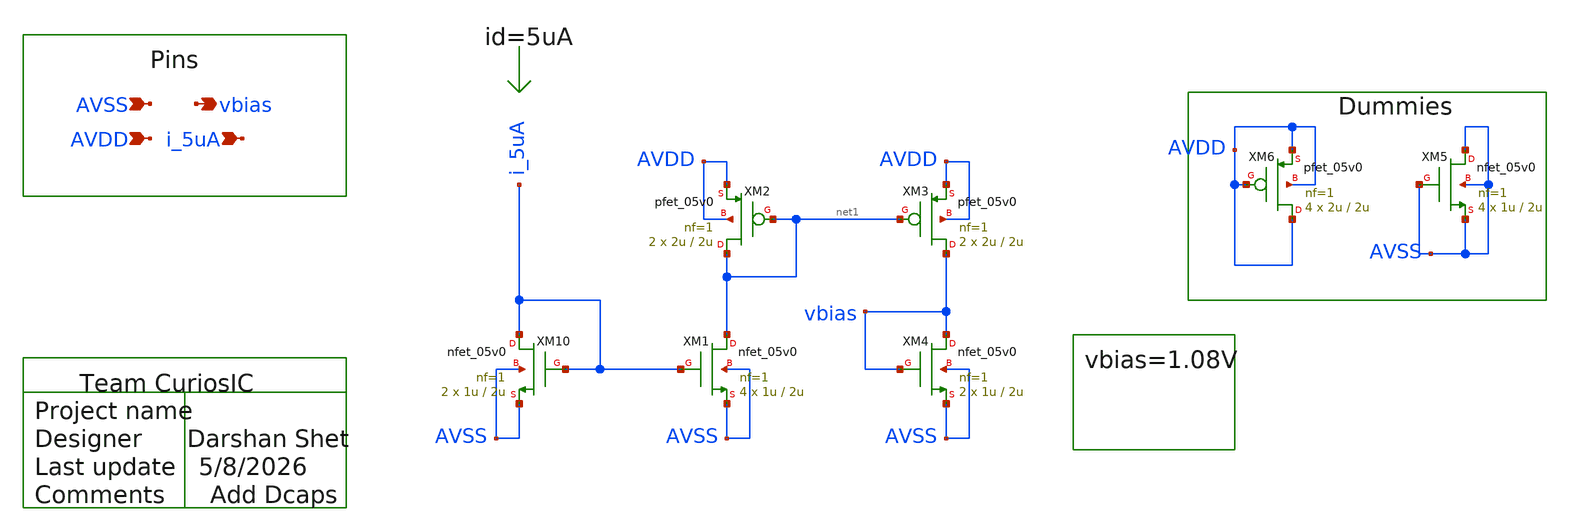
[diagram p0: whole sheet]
** sch_path: design/schematics/ADC/DSM_Loop_filter/First_int/OTA_Files/DS_cic_bms_afe_iadc_first_int_OTA_bias_ckt.sch
**.subckt DS_cic_bms_afe_iadc_first_int_OTA_bias_ckt vbias AVSS AVDD i_5uA
*.opin vbias
*.ipin AVSS
*.ipin AVDD
*.ipin i_5uA
XM10 i_5uA i_5uA AVSS AVSS nfet_05v0 L=2u W=1u nf=1 ad='int((nf+1)/2) * W/nf * 0.18u' as='int((nf+2)/2) * W/nf * 0.18u'
+ pd='2*int((nf+1)/2) * (W/nf + 0.18u)' ps='2*int((nf+2)/2) * (W/nf + 0.18u)' nrd='0.18u / W' nrs='0.18u / W'
+ sa=0 sb=0 sd=0 m=2
XM1 net1 i_5uA AVSS AVSS nfet_05v0 L=2u W=1u nf=1 ad='int((nf+1)/2) * W/nf * 0.18u' as='int((nf+2)/2) * W/nf * 0.18u'
+ pd='2*int((nf+1)/2) * (W/nf + 0.18u)' ps='2*int((nf+2)/2) * (W/nf + 0.18u)' nrd='0.18u / W' nrs='0.18u / W'
+ sa=0 sb=0 sd=0 m=4
XM2 net1 net1 AVDD AVDD pfet_05v0 L=2u W=2u nf=1 ad='int((nf+1)/2) * W/nf * 0.18u' as='int((nf+2)/2) * W/nf * 0.18u'
+ pd='2*int((nf+1)/2) * (W/nf + 0.18u)' ps='2*int((nf+2)/2) * (W/nf + 0.18u)' nrd='0.18u / W' nrs='0.18u / W'
+ sa=0 sb=0 sd=0 m=2
XM3 vbias net1 AVDD AVDD pfet_05v0 L=2u W=2u nf=1 ad='int((nf+1)/2) * W/nf * 0.18u' as='int((nf+2)/2) * W/nf * 0.18u'
+ pd='2*int((nf+1)/2) * (W/nf + 0.18u)' ps='2*int((nf+2)/2) * (W/nf + 0.18u)' nrd='0.18u / W' nrs='0.18u / W'
+ sa=0 sb=0 sd=0 m=2
XM4 vbias vbias AVSS AVSS nfet_05v0 L=2u W=1u nf=1 ad='int((nf+1)/2) * W/nf * 0.18u' as='int((nf+2)/2) * W/nf * 0.18u'
+ pd='2*int((nf+1)/2) * (W/nf + 0.18u)' ps='2*int((nf+2)/2) * (W/nf + 0.18u)' nrd='0.18u / W' nrs='0.18u / W'
+ sa=0 sb=0 sd=0 m=2
XM5 AVSS AVSS AVSS AVSS nfet_05v0 L=2u W=1u nf=1 ad='int((nf+1)/2) * W/nf * 0.18u' as='int((nf+2)/2) * W/nf * 0.18u'
+ pd='2*int((nf+1)/2) * (W/nf + 0.18u)' ps='2*int((nf+2)/2) * (W/nf + 0.18u)' nrd='0.18u / W' nrs='0.18u / W'
+ sa=0 sb=0 sd=0 m=4
XM6 AVDD AVDD AVDD AVDD pfet_05v0 L=2u W=2u nf=1 ad='int((nf+1)/2) * W/nf * 0.18u' as='int((nf+2)/2) * W/nf * 0.18u'
+ pd='2*int((nf+1)/2) * (W/nf + 0.18u)' ps='2*int((nf+2)/2) * (W/nf + 0.18u)' nrd='0.18u / W' nrs='0.18u / W'
+ sa=0 sb=0 sd=0 m=4
**.ends
.end
